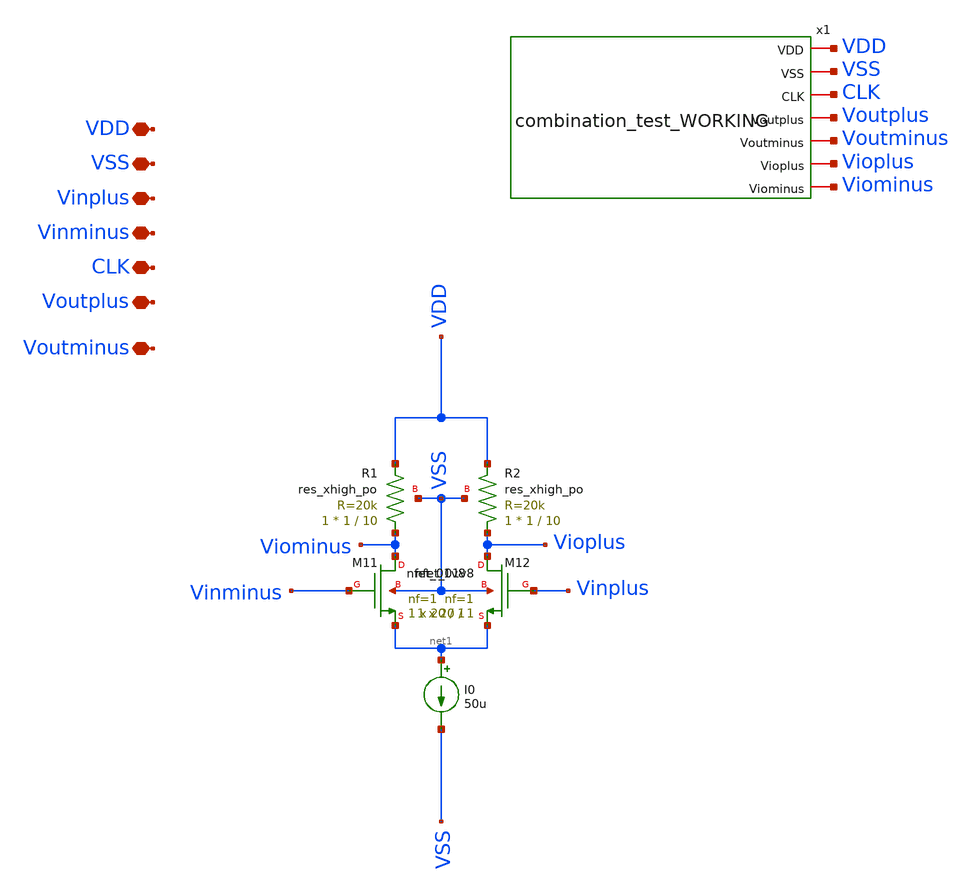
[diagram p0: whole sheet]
** sch_path: xschem/Comparator_sub.sch
**.subckt Comparator_sub VDD VSS Vinplus Vinminus CLK Voutplus Voutminus
*.iopin VDD
*.iopin VSS
*.iopin Vinplus
*.iopin Vinminus
*.iopin CLK
*.iopin Voutplus
*.iopin Voutminus
XM11 Viominus Vinminus net1 VSS sky130_fd_pr__nfet_01v8 L=1 W=20 nf=1 ad='int((nf+1)/2) * W/nf * 0.29'
+ as='int((nf+2)/2) * W/nf * 0.29' pd='2*int((nf+1)/2) * (W/nf + 0.29)' ps='2*int((nf+2)/2) * (W/nf + 0.29)'
+ nrd='0.29 / W' nrs='0.29 / W' sa=0 sb=0 sd=0 mult=1 m=1
XM12 Vioplus Vinplus net1 VSS sky130_fd_pr__nfet_01v8 L=1 W=20 nf=1 ad='int((nf+1)/2) * W/nf * 0.29'
+ as='int((nf+2)/2) * W/nf * 0.29' pd='2*int((nf+1)/2) * (W/nf + 0.29)' ps='2*int((nf+2)/2) * (W/nf + 0.29)'
+ nrd='0.29 / W' nrs='0.29 / W' sa=0 sb=0 sd=0 mult=1 m=1
I0 net1 VSS 50u
XR1 Viominus VDD VSS sky130_fd_pr__res_xhigh_po W=1 L=10 mult=1 m=1
XR2 Vioplus VDD VSS sky130_fd_pr__res_xhigh_po W=1 L=10 mult=1 m=1
x1 VDD VSS CLK Voutplus Voutminus Vioplus Viominus combination_test_WORKING
**.ends
.end
